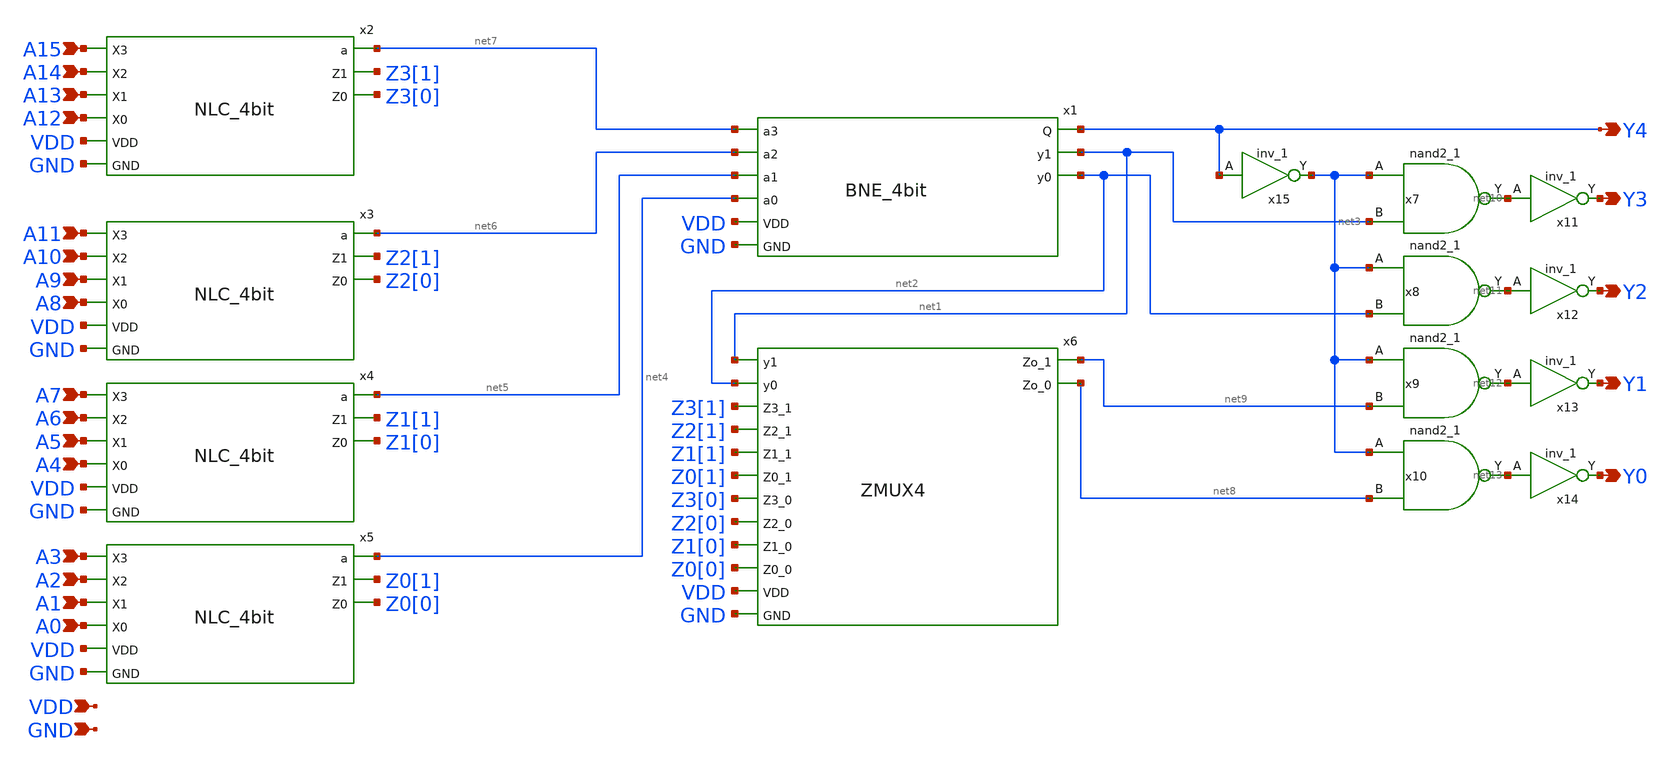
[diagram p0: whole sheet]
** sch_path: xschem/ZLC_16bit.sch
**.subckt ZLC_16bit A3 A2 A1 A0 A7 A6 A5 A4 A11 A10 A9 A8 A15 A14 A13 A12 Y4 Y3 Y2 Y1 Y0 VDD GND
*.ipin A3
*.ipin A2
*.ipin A1
*.ipin A0
*.ipin A7
*.ipin A6
*.ipin A5
*.ipin A4
*.ipin A11
*.ipin A10
*.ipin A9
*.ipin A8
*.ipin A15
*.ipin A14
*.ipin A13
*.ipin A12
*.opin Y4
*.opin Y3
*.opin Y2
*.opin Y1
*.opin Y0
*.ipin VDD
*.ipin GND
x2 A15 A14 net7 A13 A12 Z3[1] VDD Z3[0] GND NLC_4bit
x3 A11 A10 net6 A9 A8 Z2[1] VDD Z2[0] GND NLC_4bit
x4 A7 A6 net5 A5 A4 Z1[1] VDD Z1[0] GND NLC_4bit
x5 A3 A2 net4 A1 A0 Z0[1] VDD Z0[0] GND NLC_4bit
x7 net3 net1 GND GND VDD VDD net10 sky130_fd_sc_hd__nand2_1
x8 net3 net2 GND GND VDD VDD net11 sky130_fd_sc_hd__nand2_1
x9 net3 net9 GND GND VDD VDD net12 sky130_fd_sc_hd__nand2_1
x10 net3 net8 GND GND VDD VDD net13 sky130_fd_sc_hd__nand2_1
x15 Y4 GND GND VDD VDD net3 sky130_fd_sc_hd__inv_1
x11 net10 GND GND VDD VDD Y3 sky130_fd_sc_hd__inv_1
x12 net11 GND GND VDD VDD Y2 sky130_fd_sc_hd__inv_1
x13 net12 GND GND VDD VDD Y1 sky130_fd_sc_hd__inv_1
x14 net13 GND GND VDD VDD Y0 sky130_fd_sc_hd__inv_1
x1 Y4 net1 net2 net7 net6 net5 net4 VDD GND BNE_4bit
x6 net1 net2 Z3[1] Z2[1] net9 Z1[1] Z0[1] Z3[0] Z2[0] Z1[0] Z0[0] net8 VDD GND ZMUX4
**.ends

* expanding   symbol:  NLC_4bit.sym # of pins=9
** sym_path: xschem/NLC_4bit.sym
** sch_path: xschem/NLC_4bit.sch
.subckt NLC_4bit X3 X2 a X1 X0 Z1 VDD Z0 GND
*.ipin X3
*.ipin X2
*.ipin X1
*.ipin X0
*.opin a
*.opin Z1
*.opin Z0
*.ipin VDD
*.ipin GND
x1 X3 X2 X1 X0 GND GND VDD VDD a sky130_fd_sc_hd__nor4_2
x2 X3 X2 GND GND VDD VDD Z1 sky130_fd_sc_hd__nor2_1
x3 net1 X1 X3 GND GND VDD VDD Z0 sky130_fd_sc_hd__a21oi_1
x4 X2 GND GND VDD VDD net1 sky130_fd_sc_hd__inv_1
.ends


* expanding   symbol:  BNE_4bit.sym # of pins=9
** sym_path: xschem/BNE_4bit.sym
** sch_path: xschem/BNE_4bit.sch
.subckt BNE_4bit Q y1 y0 a3 a2 a1 a0 VDD GND
*.ipin a1
*.ipin a0
*.opin y1
*.opin y0
*.ipin a3
*.ipin a2
*.opin Q
*.ipin VDD
*.ipin GND
x1 a0 GND GND VDD VDD net3 sky130_fd_sc_hd__inv_1
x2 a3 GND GND VDD VDD net2 sky130_fd_sc_hd__inv_1
x3 net3 a1 GND GND VDD VDD net1 sky130_fd_sc_hd__nand2_1
x4 net1 a2 net2 GND GND VDD VDD y0 sky130_fd_sc_hd__a21oi_2
x5 a2 a3 GND GND VDD VDD net4 sky130_fd_sc_hd__nand2_1
x6 net4 GND GND VDD VDD y1 sky130_fd_sc_hd__inv_2
x7 a0 a1 GND GND VDD VDD net5 sky130_fd_sc_hd__nand2_1
x8 net5 net4 GND GND VDD VDD Q sky130_fd_sc_hd__nor2_2
.ends


* expanding   symbol:  ZMUX4.sym # of pins=14
** sym_path: xschem/ZMUX4.sym
** sch_path: xschem/ZMUX4.sch
.subckt ZMUX4 y1 y0 Z3_1 Z2_1 Zo_1 Z1_1 Z0_1 Z3_0 Z2_0 Z1_0 Z0_0 Zo_0 VDD GND
*.ipin Z0_0
*.ipin Z1_0
*.ipin y0
*.ipin Z2_0
*.ipin Z3_0
*.ipin Z0_1
*.ipin Z1_1
*.ipin Z2_1
*.ipin Z3_1
*.opin Zo_1
*.opin Zo_0
*.ipin y1
*.ipin VDD
*.ipin GND
x7 Z3_1 Z2_1 Z1_1 Z0_1 y0 y1 GND GND VDD VDD Zo_1 sky130_fd_sc_hd__mux4_1
x8 Z3_0 Z2_0 Z1_0 Z0_0 y0 y1 GND GND VDD VDD Zo_0 sky130_fd_sc_hd__mux4_1
.ends

.end
